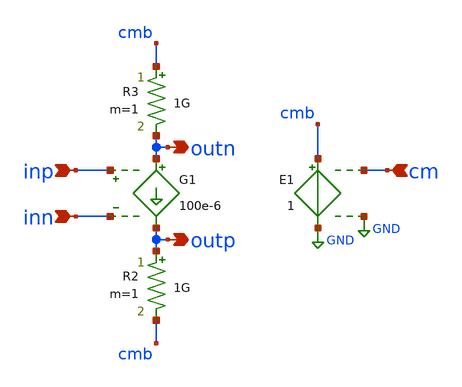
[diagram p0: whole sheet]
** sch_path: prj/template/2_Idealized_circuits/ota_gm_100u.sch
**.subckt ota_gm_100u inp inn outp outn cm
*.ipin inp
*.ipin inn
*.opin outp
*.opin outn
*.ipin cm
G1 outn outp inp inn 100e-6
R2 outp cmb 1G m=1
R3 cmb outn 1G m=1
E1 cmb GND cm GND 1
**.ends
.GLOBAL GND
.end
